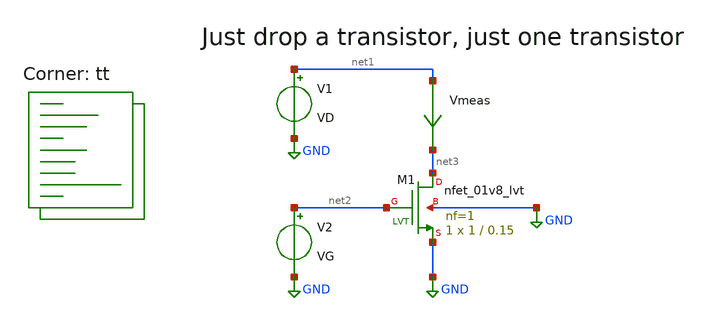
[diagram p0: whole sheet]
** sch_path: automatization_analog_design/mos_dc_characteristic/mos.sch
**.subckt mos
V1 net1 GND VD
V2 net2 GND VG
Vmeas net1 net3 0
.save i(vmeas)
XM1 net3 net2 GND GND sky130_fd_pr__nfet_01v8_lvt L=0.15 W=1 nf=1 ad='int((1 + 1)/2) * 1 / 1 * 0.29'
+ as='int((1 + 2)/2) * 1 / 1 * 0.29' pd='2*int((1 + 1)/2) * (1 / 1 + 0.29)' ps='2*int((1 + 2)/2) * (1 / 1 + 0.29)'
+ nrd='0.29 / 1 ' nrs='0.29 / 1 ' sa=0 sb=0 sd=0 mult=1 m=1
**** begin user architecture code

**************************************************************
**************************************************************
**************************************************************
**************************************************************
**************************************************************
*LIBs*********************************************************
**************************************************************
**************************************************************
**************************************************************
**************************************************************
**************************************************************
*.lib $::SKYWATER_MODELS/sky130.lib.spice tt
* chose the corners in the corner file
* tt_mm for mismatch
* ss ff sf fs standart corners
* ll hh lh hl capacitor and resistors corners
* mc for total process variation including corners
**************************************************************
**************************************************************
**************************************************************
**************************************************************
**************************************************************
*Corners/montecarlo options***********************************
**************************************************************
**************************************************************
**************************************************************
**************************************************************
**************************************************************
.TEMP 27
**************************************************************
**************************************************************
**************************************************************
**************************************************************
*SIMULATION and Plots*****************************************
**************************************************************
**************************************************************
**************************************************************
**************************************************************
.control
save all
.endc

.lib $::SKYWATER_MODELS/sky130.lib.spice tt
**** end user architecture code
**.ends
.GLOBAL GND
.end
